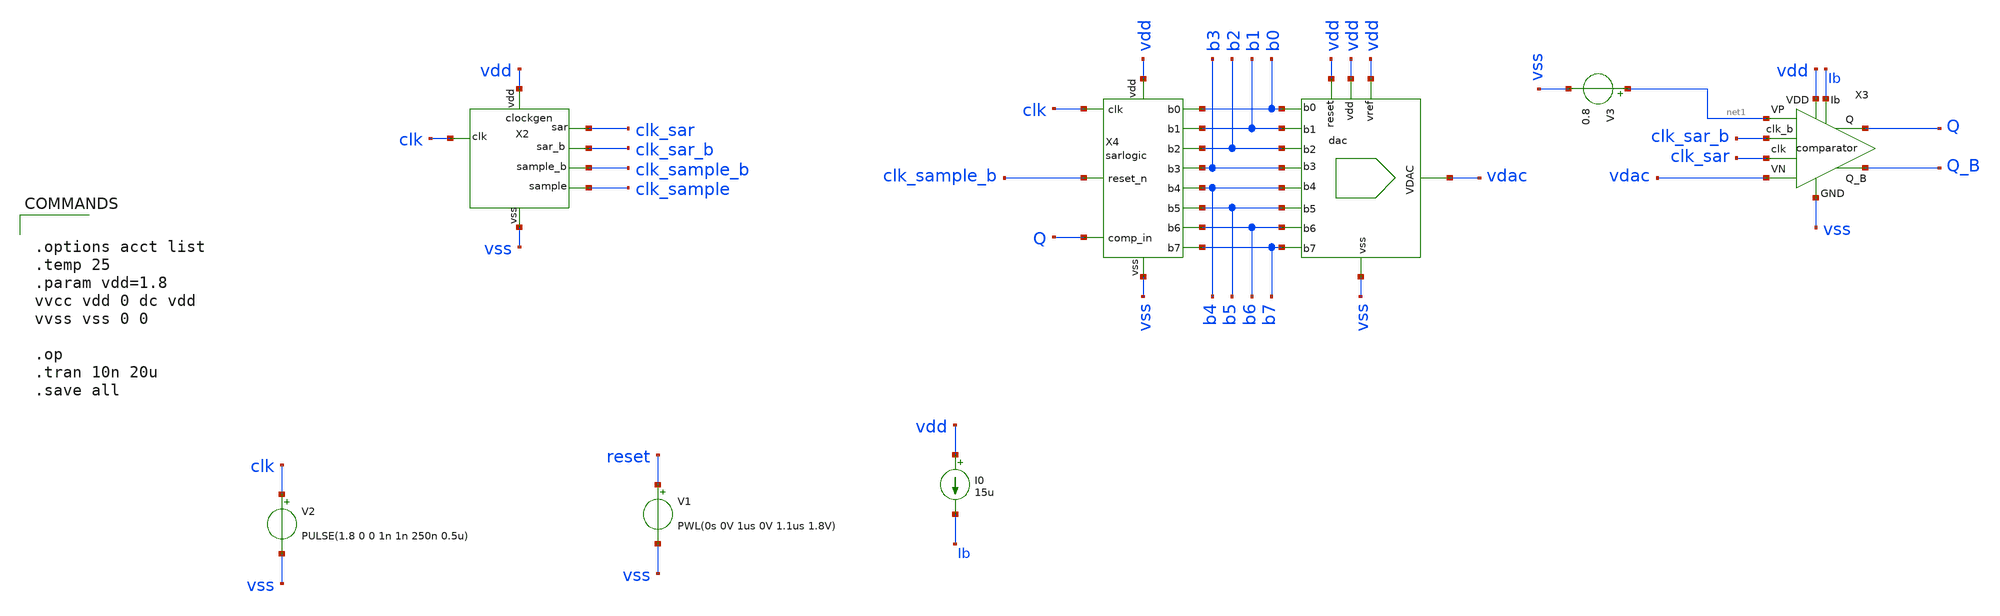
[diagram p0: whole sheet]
** sch_path: xschem/clockgen/clockgen_tb.sch
.lib $::SKYWATER_MODELS/sky130.lib.spice tt
.include $::SKYWATER_STDCELLS/sky130_fd_sc_hd.spice

**.subckt clockgen_tb
V2 clk vss PULSE(1.8 0 0 1n 1n 250n 0.5u)
X2 clk vdd clk_sar clk_sample vss clk_sar_b clk_sample_b clockgen
X4 b0 b1 clk clk_sample_b Q vdd vss b2 b3 b4 b5 b6 b7 sarlogic
V1 reset vss PWL(0s 0V 1us 0V 1.1us 1.8V)
X1 vss vdac vdd vdd b0 b1 b2 b3 b4 b5 b6 b7 vdd dac
X3 net1 vdac vss Q_B Q vdd clk_sar Ib clk_sar_b comparator
I0 vdd Ib 15u
V3 net1 vss 0.8
**** begin user architecture code


.options acct list
.temp 25
.param vdd=1.8
vvcc vdd 0 dc vdd
vvss vss 0 0

.op
.tran 10n 20u
.save all


**** end user architecture code
**.ends
.end
